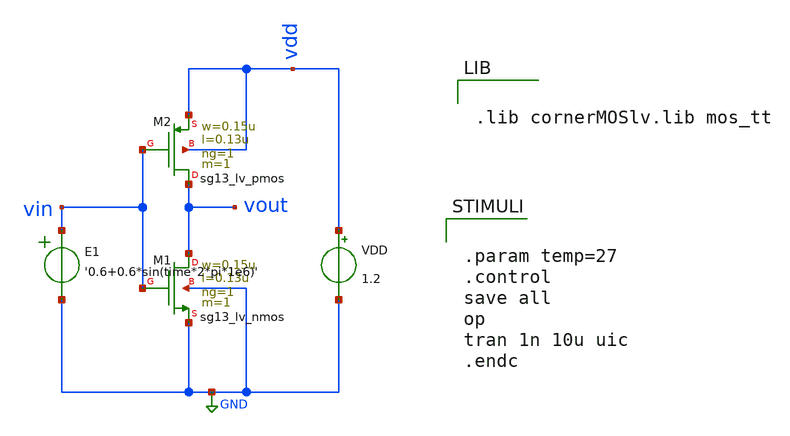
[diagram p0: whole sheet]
** sch_path: BTDay2-Ex/Ex1b_Lecture2.sch
**.subckt Ex1b_Lecture2
XM1 vout vin GND GND sg13_lv_nmos w=0.15u l=0.13u ng=1 m=1 mm_ok=1
XM2 vout vin vdd vdd sg13_lv_pmos w=0.15u l=0.13u ng=1 m=1 mm_ok=1
VDD vdd GND 1.2
E1 vin GND VOL=' '0.6+0.6*sin(time*2*pi*1e6)' '
**** begin user architecture code


.lib cornerMOSlv.lib mos_tt




.param temp=27
.control
save all
op
tran 1n 10u uic
.endc


**** end user architecture code
**.ends
.GLOBAL GND
.end
